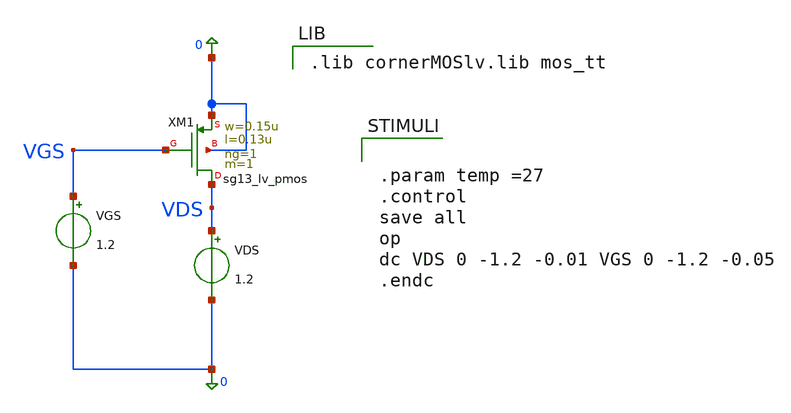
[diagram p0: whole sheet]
** sch_path: pmos_tb.sch
**.subckt pmos_tb
VDS VDS 0 1.2
VGS VGS 0 1.2
XXM1 VDS VGS 0 0 sg13_lv_pmos w=0.15u l=0.13u ng=1 m=1 mm_ok=1
**** begin user architecture code

.lib cornerMOSlv.lib mos_tt



.param temp =27
.control
save all
op
dc VDS 0 -1.2 -0.01 VGS 0 -1.2 -0.05
.endc


**** end user architecture code
**.ends
.end
